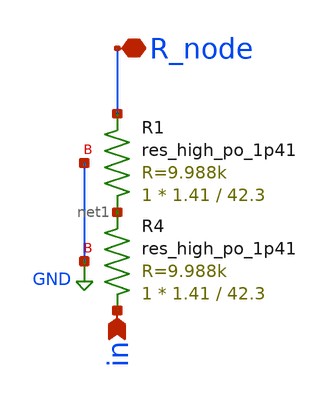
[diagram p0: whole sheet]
** sch_path: xschem/dac_sub_therm.sch
**.subckt dac_sub_therm in R_node
*.ipin in
*.iopin R_node
XR1 net1 R_node GND sky130_fd_pr__res_high_po_1p41 L=42.3 mult=1 m=1
XR4 in net1 GND sky130_fd_pr__res_high_po_1p41 L=42.3 mult=1 m=1
**.ends
.GLOBAL GND
.end
